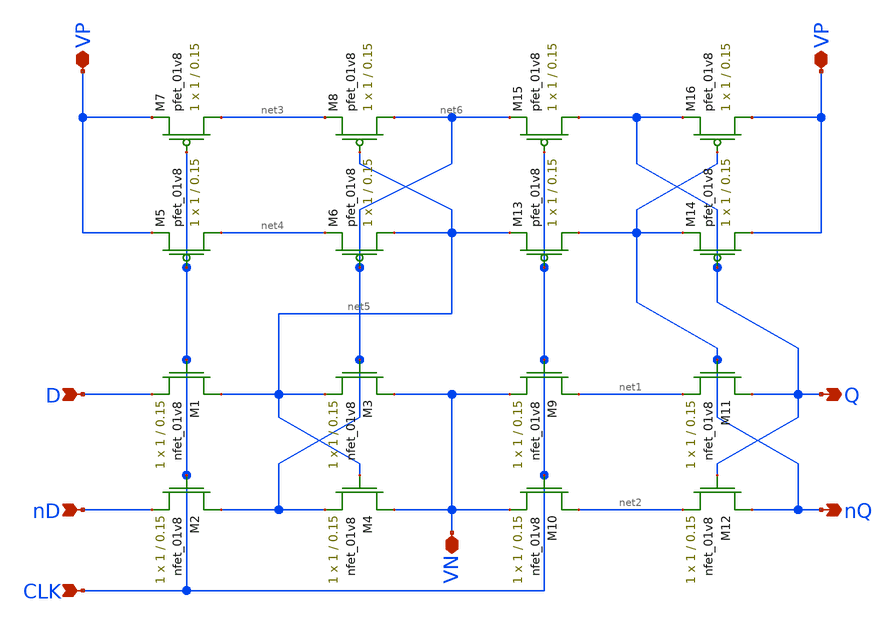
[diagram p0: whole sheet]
** sch_path: mini2/schem/dff.sch
**.subckt dff VN VP VP D nD CLK Q nQ
*.iopin VN
*.iopin VP
*.iopin VP
*.ipin D
*.ipin nD
*.ipin CLK
*.opin Q
*.opin nQ
XM1 net5 CLK D GND sky130_fd_pr__nfet_01v8 L=0.15 W=1 nf=1 ad='int((nf+1)/2) * W/nf * 0.29' as='int((nf+2)/2) * W/nf * 0.29'
+ pd='2*int((nf+1)/2) * (W/nf + 0.29)' ps='2*int((nf+2)/2) * (W/nf + 0.29)' nrd='0.29 / W' nrs='0.29 / W'
+ sa=0 sb=0 sd=0 mult=1 m=1
XM2 net6 CLK nD GND sky130_fd_pr__nfet_01v8 L=0.15 W=1 nf=1 ad='int((nf+1)/2) * W/nf * 0.29' as='int((nf+2)/2) * W/nf * 0.29'
+ pd='2*int((nf+1)/2) * (W/nf + 0.29)' ps='2*int((nf+2)/2) * (W/nf + 0.29)' nrd='0.29 / W' nrs='0.29 / W'
+ sa=0 sb=0 sd=0 mult=1 m=1
XM3 VN net6 net5 GND sky130_fd_pr__nfet_01v8 L=0.15 W=1 nf=1 ad='int((nf+1)/2) * W/nf * 0.29' as='int((nf+2)/2) * W/nf * 0.29'
+ pd='2*int((nf+1)/2) * (W/nf + 0.29)' ps='2*int((nf+2)/2) * (W/nf + 0.29)' nrd='0.29 / W' nrs='0.29 / W'
+ sa=0 sb=0 sd=0 mult=1 m=1
XM4 VN net5 net6 GND sky130_fd_pr__nfet_01v8 L=0.15 W=1 nf=1 ad='int((nf+1)/2) * W/nf * 0.29' as='int((nf+2)/2) * W/nf * 0.29'
+ pd='2*int((nf+1)/2) * (W/nf + 0.29)' ps='2*int((nf+2)/2) * (W/nf + 0.29)' nrd='0.29 / W' nrs='0.29 / W'
+ sa=0 sb=0 sd=0 mult=1 m=1
XM5 net4 CLK VP VDD sky130_fd_pr__pfet_01v8 L=0.15 W=1 nf=1 ad='int((nf+1)/2) * W/nf * 0.29' as='int((nf+2)/2) * W/nf * 0.29'
+ pd='2*int((nf+1)/2) * (W/nf + 0.29)' ps='2*int((nf+2)/2) * (W/nf + 0.29)' nrd='0.29 / W' nrs='0.29 / W'
+ sa=0 sb=0 sd=0 mult=1 m=1
XM6 net5 net6 net4 VDD sky130_fd_pr__pfet_01v8 L=0.15 W=1 nf=1 ad='int((nf+1)/2) * W/nf * 0.29' as='int((nf+2)/2) * W/nf * 0.29'
+ pd='2*int((nf+1)/2) * (W/nf + 0.29)' ps='2*int((nf+2)/2) * (W/nf + 0.29)' nrd='0.29 / W' nrs='0.29 / W'
+ sa=0 sb=0 sd=0 mult=1 m=1
XM7 net3 CLK VP VDD sky130_fd_pr__pfet_01v8 L=0.15 W=1 nf=1 ad='int((nf+1)/2) * W/nf * 0.29' as='int((nf+2)/2) * W/nf * 0.29'
+ pd='2*int((nf+1)/2) * (W/nf + 0.29)' ps='2*int((nf+2)/2) * (W/nf + 0.29)' nrd='0.29 / W' nrs='0.29 / W'
+ sa=0 sb=0 sd=0 mult=1 m=1
XM8 net6 net5 net3 VDD sky130_fd_pr__pfet_01v8 L=0.15 W=1 nf=1 ad='int((nf+1)/2) * W/nf * 0.29' as='int((nf+2)/2) * W/nf * 0.29'
+ pd='2*int((nf+1)/2) * (W/nf + 0.29)' ps='2*int((nf+2)/2) * (W/nf + 0.29)' nrd='0.29 / W' nrs='0.29 / W'
+ sa=0 sb=0 sd=0 mult=1 m=1
XM9 net1 CLK VN GND sky130_fd_pr__nfet_01v8 L=0.15 W=1 nf=1 ad='int((nf+1)/2) * W/nf * 0.29' as='int((nf+2)/2) * W/nf * 0.29'
+ pd='2*int((nf+1)/2) * (W/nf + 0.29)' ps='2*int((nf+2)/2) * (W/nf + 0.29)' nrd='0.29 / W' nrs='0.29 / W'
+ sa=0 sb=0 sd=0 mult=1 m=1
XM10 net2 CLK VN GND sky130_fd_pr__nfet_01v8 L=0.15 W=1 nf=1 ad='int((nf+1)/2) * W/nf * 0.29' as='int((nf+2)/2) * W/nf * 0.29'
+ pd='2*int((nf+1)/2) * (W/nf + 0.29)' ps='2*int((nf+2)/2) * (W/nf + 0.29)' nrd='0.29 / W' nrs='0.29 / W'
+ sa=0 sb=0 sd=0 mult=1 m=1
XM11 Q nQ net1 GND sky130_fd_pr__nfet_01v8 L=0.15 W=1 nf=1 ad='int((nf+1)/2) * W/nf * 0.29' as='int((nf+2)/2) * W/nf * 0.29'
+ pd='2*int((nf+1)/2) * (W/nf + 0.29)' ps='2*int((nf+2)/2) * (W/nf + 0.29)' nrd='0.29 / W' nrs='0.29 / W'
+ sa=0 sb=0 sd=0 mult=1 m=1
XM12 nQ Q net2 GND sky130_fd_pr__nfet_01v8 L=0.15 W=1 nf=1 ad='int((nf+1)/2) * W/nf * 0.29' as='int((nf+2)/2) * W/nf * 0.29'
+ pd='2*int((nf+1)/2) * (W/nf + 0.29)' ps='2*int((nf+2)/2) * (W/nf + 0.29)' nrd='0.29 / W' nrs='0.29 / W'
+ sa=0 sb=0 sd=0 mult=1 m=1
XM13 nQ CLK net5 VDD sky130_fd_pr__pfet_01v8 L=0.15 W=1 nf=1 ad='int((nf+1)/2) * W/nf * 0.29' as='int((nf+2)/2) * W/nf * 0.29'
+ pd='2*int((nf+1)/2) * (W/nf + 0.29)' ps='2*int((nf+2)/2) * (W/nf + 0.29)' nrd='0.29 / W' nrs='0.29 / W'
+ sa=0 sb=0 sd=0 mult=1 m=1
XM14 VP Q nQ VDD sky130_fd_pr__pfet_01v8 L=0.15 W=1 nf=1 ad='int((nf+1)/2) * W/nf * 0.29' as='int((nf+2)/2) * W/nf * 0.29'
+ pd='2*int((nf+1)/2) * (W/nf + 0.29)' ps='2*int((nf+2)/2) * (W/nf + 0.29)' nrd='0.29 / W' nrs='0.29 / W'
+ sa=0 sb=0 sd=0 mult=1 m=1
XM15 Q CLK net6 VDD sky130_fd_pr__pfet_01v8 L=0.15 W=1 nf=1 ad='int((nf+1)/2) * W/nf * 0.29' as='int((nf+2)/2) * W/nf * 0.29'
+ pd='2*int((nf+1)/2) * (W/nf + 0.29)' ps='2*int((nf+2)/2) * (W/nf + 0.29)' nrd='0.29 / W' nrs='0.29 / W'
+ sa=0 sb=0 sd=0 mult=1 m=1
XM16 VP nQ Q VDD sky130_fd_pr__pfet_01v8 L=0.15 W=1 nf=1 ad='int((nf+1)/2) * W/nf * 0.29' as='int((nf+2)/2) * W/nf * 0.29'
+ pd='2*int((nf+1)/2) * (W/nf + 0.29)' ps='2*int((nf+2)/2) * (W/nf + 0.29)' nrd='0.29 / W' nrs='0.29 / W'
+ sa=0 sb=0 sd=0 mult=1 m=1
**.ends
.end
